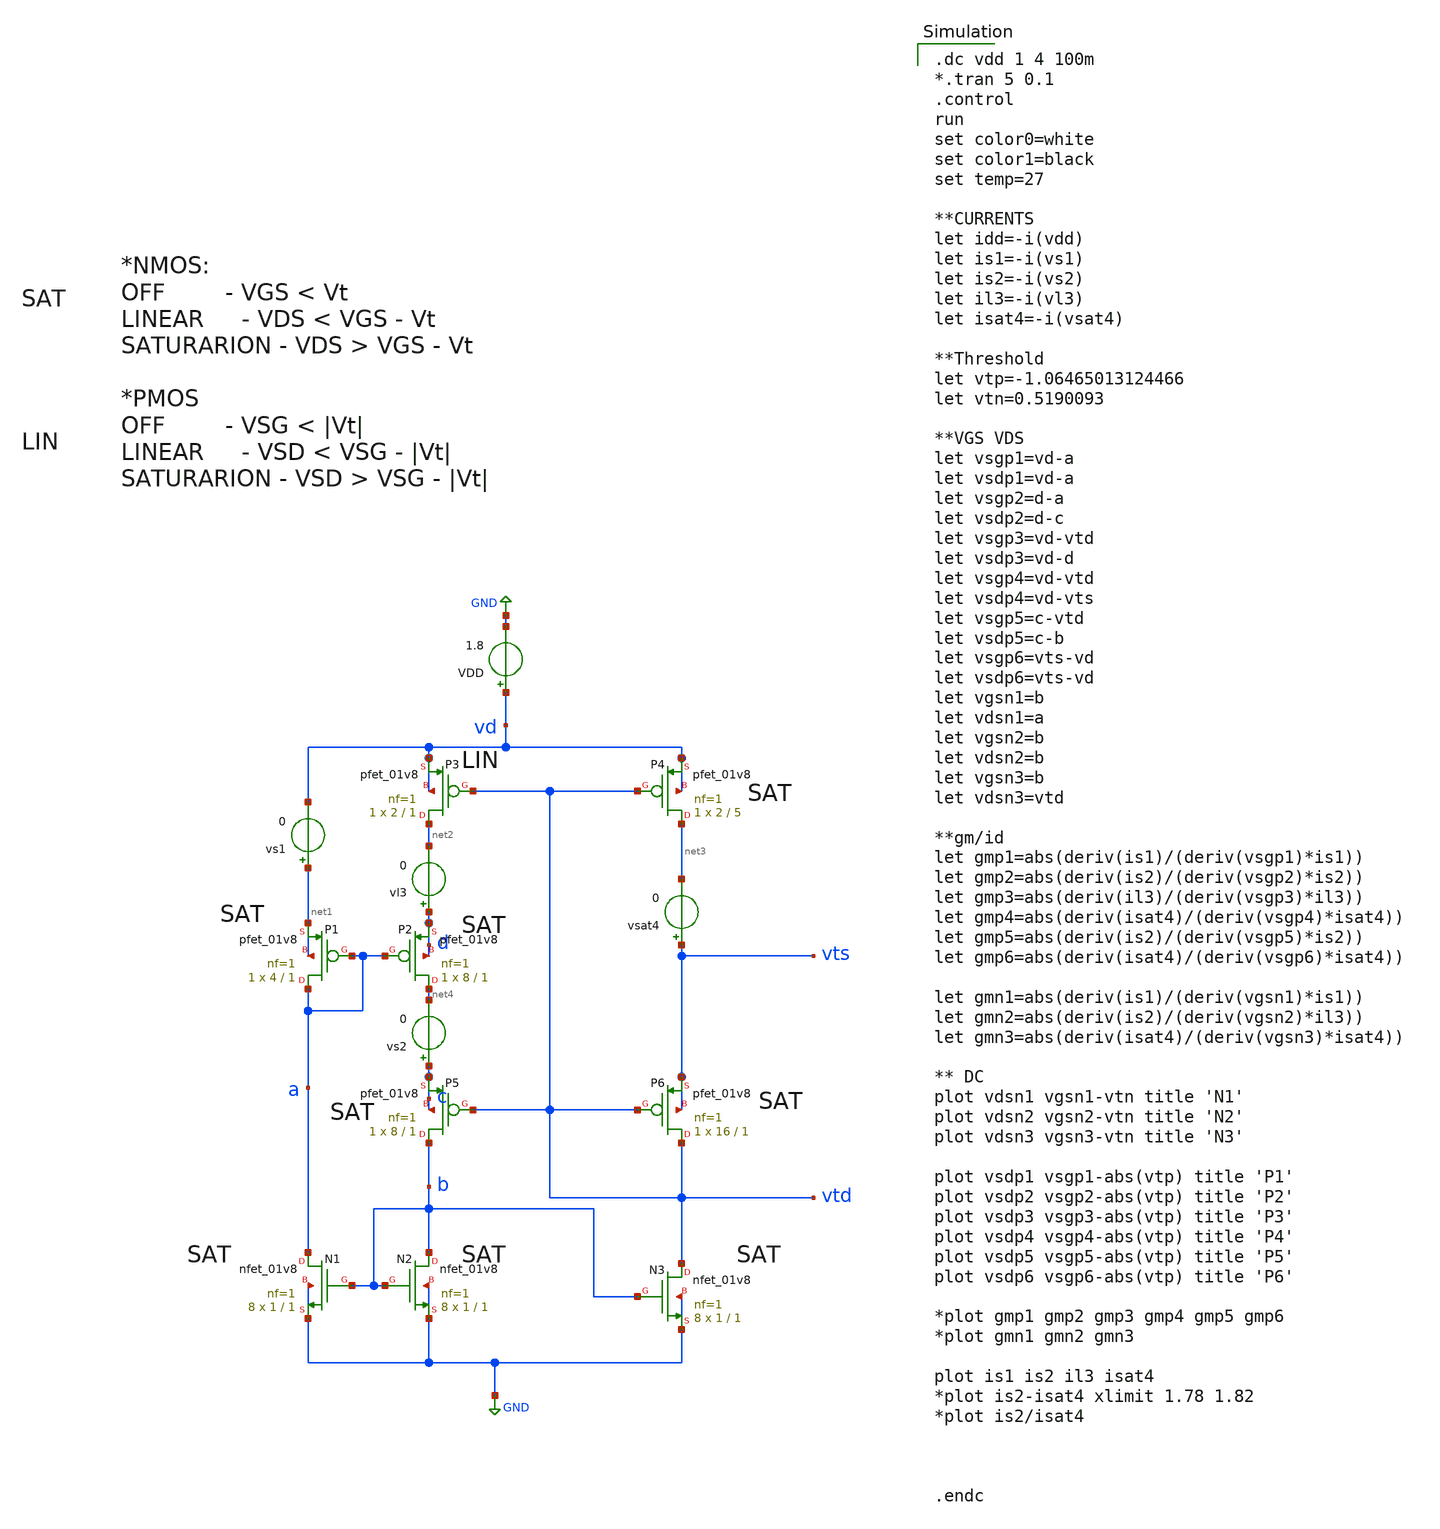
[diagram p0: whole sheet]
** sch_path: sensor/xschem/temp-tb-dc.sch
**.subckt temp-tb-dc
VDD vd GND 1.8
vs1 net1 vd 0
vs2 c net4 0
vl3 d net2 0
vsat4 vts net3 0
XP1 a a net1 net1 sky130_fd_pr__pfet_01v8 L=1 W=4 nf=1 ad='int((nf+1)/2) * W/nf * 0.29' as='int((nf+2)/2) * W/nf * 0.29'
+ pd='2*int((nf+1)/2) * (W/nf + 0.29)' ps='2*int((nf+2)/2) * (W/nf + 0.29)' nrd='0.29 / W' nrs='0.29 / W'
+ sa=0 sb=0 sd=0 mult=1 m=1
XP2 net4 a d d sky130_fd_pr__pfet_01v8 L=1 W=8 nf=1 ad='int((nf+1)/2) * W/nf * 0.29' as='int((nf+2)/2) * W/nf * 0.29'
+ pd='2*int((nf+1)/2) * (W/nf + 0.29)' ps='2*int((nf+2)/2) * (W/nf + 0.29)' nrd='0.29 / W' nrs='0.29 / W'
+ sa=0 sb=0 sd=0 mult=1 m=1
XP3 net2 vtd vd vd sky130_fd_pr__pfet_01v8 L=1 W=2 nf=1 ad='int((nf+1)/2) * W/nf * 0.29' as='int((nf+2)/2) * W/nf * 0.29'
+ pd='2*int((nf+1)/2) * (W/nf + 0.29)' ps='2*int((nf+2)/2) * (W/nf + 0.29)' nrd='0.29 / W' nrs='0.29 / W'
+ sa=0 sb=0 sd=0 mult=1 m=1
XP4 net3 vtd vd vd sky130_fd_pr__pfet_01v8 L=5 W=2 nf=1 ad='int((nf+1)/2) * W/nf * 0.29' as='int((nf+2)/2) * W/nf * 0.29'
+ pd='2*int((nf+1)/2) * (W/nf + 0.29)' ps='2*int((nf+2)/2) * (W/nf + 0.29)' nrd='0.29 / W' nrs='0.29 / W'
+ sa=0 sb=0 sd=0 mult=1 m=1
XP5 b vtd c c sky130_fd_pr__pfet_01v8 L=1 W=8 nf=1 ad='int((nf+1)/2) * W/nf * 0.29' as='int((nf+2)/2) * W/nf * 0.29'
+ pd='2*int((nf+1)/2) * (W/nf + 0.29)' ps='2*int((nf+2)/2) * (W/nf + 0.29)' nrd='0.29 / W' nrs='0.29 / W'
+ sa=0 sb=0 sd=0 mult=1 m=1
XP6 vtd vtd vts vts sky130_fd_pr__pfet_01v8 L=1 W=16 nf=1 ad='int((nf+1)/2) * W/nf * 0.29' as='int((nf+2)/2) * W/nf * 0.29'
+ pd='2*int((nf+1)/2) * (W/nf + 0.29)' ps='2*int((nf+2)/2) * (W/nf + 0.29)' nrd='0.29 / W' nrs='0.29 / W'
+ sa=0 sb=0 sd=0 mult=1 m=1
XN1 a b GND GND sky130_fd_pr__nfet_01v8 L=1 W=1 nf=1 ad='int((nf+1)/2) * W/nf * 0.29' as='int((nf+2)/2) * W/nf * 0.29'
+ pd='2*int((nf+1)/2) * (W/nf + 0.29)' ps='2*int((nf+2)/2) * (W/nf + 0.29)' nrd='0.29 / W' nrs='0.29 / W'
+ sa=0 sb=0 sd=0 mult=8 m=8
XN2 b b GND GND sky130_fd_pr__nfet_01v8 L=1 W=1 nf=1 ad='int((nf+1)/2) * W/nf * 0.29' as='int((nf+2)/2) * W/nf * 0.29'
+ pd='2*int((nf+1)/2) * (W/nf + 0.29)' ps='2*int((nf+2)/2) * (W/nf + 0.29)' nrd='0.29 / W' nrs='0.29 / W'
+ sa=0 sb=0 sd=0 mult=8 m=8
XN3 vtd b GND GND sky130_fd_pr__nfet_01v8 L=1 W=1 nf=1 ad='int((nf+1)/2) * W/nf * 0.29' as='int((nf+2)/2) * W/nf * 0.29'
+ pd='2*int((nf+1)/2) * (W/nf + 0.29)' ps='2*int((nf+2)/2) * (W/nf + 0.29)' nrd='0.29 / W' nrs='0.29 / W'
+ sa=0 sb=0 sd=0 mult=8 m=8
**** begin user architecture code

.dc vdd 1 4 100m
*.tran 5 0.1
.control
run
set color0=white
set color1=black
set temp=27

**CURRENTS
let idd=-i(vdd)
let is1=-i(vs1)
let is2=-i(vs2)
let il3=-i(vl3)
let isat4=-i(vsat4)

**Threshold
let vtp=-1.06465013124466
let vtn=0.5190093

**VGS VDS
let vsgp1=vd-a
let vsdp1=vd-a
let vsgp2=d-a
let vsdp2=d-c
let vsgp3=vd-vtd
let vsdp3=vd-d
let vsgp4=vd-vtd
let vsdp4=vd-vts
let vsgp5=c-vtd
let vsdp5=c-b
let vsgp6=vts-vd
let vsdp6=vts-vd
let vgsn1=b
let vdsn1=a
let vgsn2=b
let vdsn2=b
let vgsn3=b
let vdsn3=vtd

**gm/id
let gmp1=abs(deriv(is1)/(deriv(vsgp1)*is1))
let gmp2=abs(deriv(is2)/(deriv(vsgp2)*is2))
let gmp3=abs(deriv(il3)/(deriv(vsgp3)*il3))
let gmp4=abs(deriv(isat4)/(deriv(vsgp4)*isat4))
let gmp5=abs(deriv(is2)/(deriv(vsgp5)*is2))
let gmp6=abs(deriv(isat4)/(deriv(vsgp6)*isat4))

let gmn1=abs(deriv(is1)/(deriv(vgsn1)*is1))
let gmn2=abs(deriv(is2)/(deriv(vgsn2)*il3))
let gmn3=abs(deriv(isat4)/(deriv(vgsn3)*isat4))

** DC
plot vdsn1 vgsn1-vtn title 'N1'
plot vdsn2 vgsn2-vtn title 'N2'
plot vdsn3 vgsn3-vtn title 'N3'

plot vsdp1 vsgp1-abs(vtp) title 'P1'
plot vsdp2 vsgp2-abs(vtp) title 'P2'
plot vsdp3 vsgp3-abs(vtp) title 'P3'
plot vsdp4 vsgp4-abs(vtp) title 'P4'
plot vsdp5 vsgp5-abs(vtp) title 'P5'
plot vsdp6 vsgp6-abs(vtp) title 'P6'

*plot gmp1 gmp2 gmp3 gmp4 gmp5 gmp6
*plot gmn1 gmn2 gmn3

plot is1 is2 il3 isat4
*plot is2-isat4 xlimit 1.78 1.82
*plot is2/isat4



.endc



.lib /home/hugodg/sky130_workspace/skywater-pdk/libraries/sky130_fd_pr_ngspice/latest/models/sky130.lib.spice tt



R0 a.t0 a.t2 322.956
R1 a.n0 a.t0 112.107
R2 a.n0 a.t1 8.249
R3 a a.n0 0.37
R4 vd.n16 vd.n15 373.459
R5 vd.n17 vd.n16 237.354
R6 vd.n8 vd.n7 104.028
R7 vd.n1 vd.n0 103.152
R8 vd.n18 vd.n17 2.481
R9 vd vd.n19 1.401
R10 vd.n19 vd.n9 0.584
R11 vd.n9 vd.n8 0.381
R12 vd.n9 vd.n1 0.329
R13 vd.n19 vd.n18 0.196
R14 vd.n7 vd.n6 0.015
R15 vd.n3 vd.n2 0.008
R16 vd.n15 vd.n14 0.008
R17 vd.n4 vd.n3 0.007
R18 vd.n16 vd.n13 0.007
R19 vd.n11 vd.n10 0.004
R20 vd.n12 vd.n11 0.003
R21 vd.n5 vd.n4 0.002
R22 vd.n13 vd.n12 0.002
R23 vd.n8 vd.n5 0.001
R24 b.n22 b.t16 38.16
R25 b.n1 b.t24 38.157
R26 b.n8 b.t14 38.143
R27 b.n27 b.t22 37.37
R28 b.n26 b.t18 37.37
R29 b.n25 b.t23 37.37
R30 b.n23 b.t21 37.37
R31 b.n12 b.t10 37.37
R32 b.n6 b.t30 37.37
R33 b.n5 b.t26 37.37
R34 b.n4 b.t31 37.37
R35 b.n2 b.t29 37.37
R36 b.n7 b.t27 37.369
R37 b.n13 b.t2 37.369
R38 b.n11 b.t0 37.369
R39 b.n9 b.t4 37.369
R40 b.n24 b.t17 37.369
R41 b.n22 b.t20 37.369
R42 b.n10 b.t12 37.369
R43 b.n8 b.t6 37.369
R44 b.n3 b.t25 37.369
R45 b.n1 b.t28 37.369
R46 b.n28 b.t19 37.362
R47 b.n0 b.t8 37.358
R48 b.n14 b.t15 18.134
R49 b.n14 b.t7 17.404
R50 b.n15 b.t5 17.404
R51 b.n16 b.t13 17.404
R52 b.n17 b.t1 17.404
R53 b.n18 b.t11 17.404
R54 b.n19 b.t3 17.404
R55 b.n20 b.t9 17.404
R56 b.n0 b.n7 1.125
R57 b.n28 b.n27 0.84
R58 b.n7 b.n6 0.832
R59 b.n24 b.n23 0.831
R60 b.n3 b.n2 0.828
R61 b.n0 b.n13 0.815
R62 b.n10 b.n9 0.814
R63 b.n26 b.n25 0.806
R64 b.n12 b.n11 0.789
R65 b.n5 b.n4 0.785
R66 b.n27 b.n26 0.773
R67 b.n13 b.n12 0.773
R68 b.n6 b.n5 0.772
R69 b.n11 b.n10 0.742
R70 b.n4 b.n3 0.739
R71 b.n23 b.n22 0.738
R72 b.n9 b.n8 0.738
R73 b.n2 b.n1 0.735
R74 b.n20 b.n19 0.73
R75 b.n19 b.n18 0.73
R76 b.n18 b.n17 0.73
R77 b.n17 b.n16 0.73
R78 b.n16 b.n15 0.73
R79 b.n15 b.n14 0.73
R80 b.n25 b.n24 0.709
R81 b b.n28 0.567
R82 b.n21 b.n0 0.287
R83 b b.n21 0.281
R84 b.n21 b.n20 0.229
R85 gnd.n15 gnd.n4 1.172
R86 gnd.n15 gnd.n9 1.13
R87 gnd.n4 gnd.n2 0.337
R88 gnd.n9 gnd.n7 0.337
R89 gnd.n14 gnd.n12 0.337
R90 gnd gnd.n15 0.143
R91 gnd.n15 gnd.n14 0.128
R92 gnd.n9 gnd.n8 0.046
R93 gnd.n4 gnd.n3 0.046
R94 gnd.n14 gnd.n13 0.046
R95 gnd.n2 gnd.n1 0.001
R96 gnd.n7 gnd.n6 0.001
R97 gnd.n12 gnd.n11 0.001
R98 gnd.n6 gnd.n5 0.001
R99 gnd.n1 gnd.n0 0.001
R100 gnd.n11 gnd.n10 0.001
R101 vtd.n0 vtd.t0 401.028
R102 vtd.n2 vtd.t2 211.175
R103 vtd.n2 vtd.t4 69.741
R104 vtd.n1 vtd.t3 18.046
R105 vtd.n0 vtd.t1 6.301
R106 vtd.n1 vtd.n0 3.191
R107 vtd vtd.n1 0.937
R108 vtd vtd.n2 0.479
R109 vts.n8 vts.n7 107.805
R110 vts.n2 vts.n1 103.152
R111 vts.n9 vts.n8 4.188
R112 vts vts.n9 1.049
R113 vts.n9 vts.n2 0.334
R114 vts.n1 vts.n0 0.015
R115 vts.n5 vts.n4 0.001
R116 vts.n4 vts.n3 0.001
R117 vts.n6 vts.n5 0.001
R118 vts.n8 vts.n6 0.001
C0 vtd vts 0.44fF
C1 vtd a 0.48fF
C2 a d 0.38fF
C3 a b 1.77fF
C4 vd c 0.07fF
C5 vd vtd 0.34fF
C6 vd d 0.40fF
C7 vd b 0.21fF
C8 gnd a 1.16fF
C9 c vtd 0.60fF
C10 c d 0.97fF
C11 c b 0.60fF
C12 vtd d 0.94fF
C13 vd gnd 0.99fF
C14 vtd b 1.83fF
C15 d b 0.30fF
C16 gnd c 1.73fF
C17 vd vts 0.33fF
C18 vd a 0.68fF
C19 gnd vtd 1.80fF
C20 c a 0.58fF
C21 gnd d 0.25fF
C22 gnd b 6.93fF
C23 vts.n0 0 2.26fF $ **FLOATING
C24 vts.n1 0 0.14fF $ **FLOATING
C25 vts.n2 0 0.14fF $ **FLOATING
C26 vts.n3 0 0.25fF $ **FLOATING
C27 vts.n4 0 0.25fF $ **FLOATING
C28 vts.n6 0 4.25fF $ **FLOATING
C29 vts.n7 0 2.41fF $ **FLOATING
C30 vts.n8 0 0.54fF $ **FLOATING
C31 vts.n9 0 2.05fF $ **FLOATING
C32 vtd.t3 0 5.31fF
C33 vtd.t0 0 4.79fF
C34 vtd.t1 0 2.80fF
C35 vtd.n0 0 3.49fF $ **FLOATING
C36 vtd.n1 0 2.77fF $ **FLOATING
C37 vtd.t4 0 1.03fF
C38 vtd.t2 0 2.67fF
C39 vtd.n2 0 8.47fF $ **FLOATING
C40 gnd.n0 0 11.88fF $ **FLOATING
C41 gnd.n1 0 0.03fF $ **FLOATING
C42 gnd.n2 0 0.22fF $ **FLOATING
C43 gnd.n3 0 0.16fF $ **FLOATING
C44 gnd.n4 0 1.85fF $ **FLOATING
C45 gnd.n5 0 11.88fF $ **FLOATING
C46 gnd.n6 0 0.03fF $ **FLOATING
C47 gnd.n7 0 0.22fF $ **FLOATING
C48 gnd.n8 0 0.16fF $ **FLOATING
C49 gnd.n9 0 1.84fF $ **FLOATING
C50 gnd.n10 0 11.88fF $ **FLOATING
C51 gnd.n11 0 0.03fF $ **FLOATING
C52 gnd.n12 0 0.22fF $ **FLOATING
C53 gnd.n13 0 0.16fF $ **FLOATING
C54 gnd.n14 0 1.77fF $ **FLOATING
C55 gnd.n15 0 0.29fF $ **FLOATING
C56 b.n0 0 2.60fF $ **FLOATING
C57 b.t24 0 2.38fF
C58 b.t28 0 2.33fF
C59 b.n1 0 4.55fF $ **FLOATING
C60 b.t29 0 2.34fF
C61 b.n2 0 2.47fF $ **FLOATING
C62 b.t25 0 2.33fF
C63 b.n3 0 2.47fF $ **FLOATING
C64 b.t31 0 2.33fF
C65 b.n4 0 2.44fF $ **FLOATING
C66 b.t26 0 2.33fF
C67 b.n5 0 2.43fF $ **FLOATING
C68 b.t30 0 2.33fF
C69 b.n6 0 2.48fF $ **FLOATING
C70 b.t27 0 2.33fF
C71 b.n7 0 2.64fF $ **FLOATING
C72 b.t8 0 2.33fF
C73 b.t14 0 2.38fF
C74 b.t6 0 2.33fF
C75 b.n8 0 4.62fF $ **FLOATING
C76 b.t4 0 2.33fF
C77 b.n9 0 2.55fF $ **FLOATING
C78 b.t12 0 2.33fF
C79 b.n10 0 2.46fF $ **FLOATING
C80 b.t0 0 2.33fF
C81 b.n11 0 2.54fF $ **FLOATING
C82 b.t10 0 2.33fF
C83 b.n12 0 2.45fF $ **FLOATING
C84 b.t2 0 2.33fF
C85 b.n13 0 2.57fF $ **FLOATING
C86 b.t9 0 0.10fF
C87 b.t3 0 0.10fF
C88 b.t11 0 0.10fF
C89 b.t1 0 0.10fF
C90 b.t13 0 0.10fF
C91 b.t5 0 0.10fF
C92 b.t7 0 0.10fF
C93 b.t15 0 0.15fF
C94 b.n14 0 2.89fF $ **FLOATING
C95 b.n15 0 1.59fF $ **FLOATING
C96 b.n16 0 1.59fF $ **FLOATING
C97 b.n17 0 1.59fF $ **FLOATING
C98 b.n18 0 1.59fF $ **FLOATING
C99 b.n19 0 1.59fF $ **FLOATING
C100 b.n20 0 1.29fF $ **FLOATING
C101 b.n21 0 0.48fF $ **FLOATING
C102 b.t16 0 2.38fF
C103 b.t20 0 2.33fF
C104 b.n22 0 4.53fF $ **FLOATING
C105 b.t21 0 2.33fF
C106 b.n23 0 2.46fF $ **FLOATING
C107 b.t17 0 2.33fF
C108 b.n24 0 10.09fF $ **FLOATING
C109 b.t23 0 2.33fF
C110 b.n25 0 3.69fF $ **FLOATING
C111 b.t18 0 2.33fF
C112 b.n26 0 2.46fF $ **FLOATING
C113 b.t22 0 2.33fF
C114 b.n27 0 2.48fF $ **FLOATING
C115 b.t19 0 2.33fF
C116 b.n28 0 2.30fF $ **FLOATING
C117 vd.n0 0 0.93fF $ **FLOATING
C118 vd.n1 0 0.08fF $ **FLOATING
C119 vd.n2 0 0.11fF $ **FLOATING
C120 vd.n3 0 0.11fF $ **FLOATING
C121 vd.n5 0 1.31fF $ **FLOATING
C122 vd.n6 0 0.85fF $ **FLOATING
C123 vd.n7 0 0.08fF $ **FLOATING
C124 vd.n8 0 0.16fF $ **FLOATING
C125 vd.n9 0 0.40fF $ **FLOATING
C126 vd.n10 0 0.15fF $ **FLOATING
C127 vd.n11 0 0.18fF $ **FLOATING
C128 vd.n12 0 1.42fF $ **FLOATING
C129 vd.n13 0 1.51fF $ **FLOATING
C130 vd.n14 0 1.83fF $ **FLOATING
C131 vd.n15 0 0.18fF $ **FLOATING
C132 vd.n16 0 0.24fF $ **FLOATING
C133 vd.n17 0 2.11fF $ **FLOATING
C134 vd.n18 0 0.45fF $ **FLOATING
C135 vd.n19 0 1.06fF $ **FLOATING
C136 a.t2 0 5.44fF
C137 a.t0 0 3.68fF
C138 a.t1 0 0.35fF
C139 a.n0 0 2.53fF $ **FLOATING
C140 vd 0 21.61fF
C141 vts 0 9.34fF
C142 vtd 0 23.19fF
C143 gnd 0 33.15fF
C144 b 0 130.37fF
C145 c 0 4.17fF
C146 d 0 22.81fF
C147 a 0 23.94fF



**** end user architecture code
**.ends
.GLOBAL GND
.end
